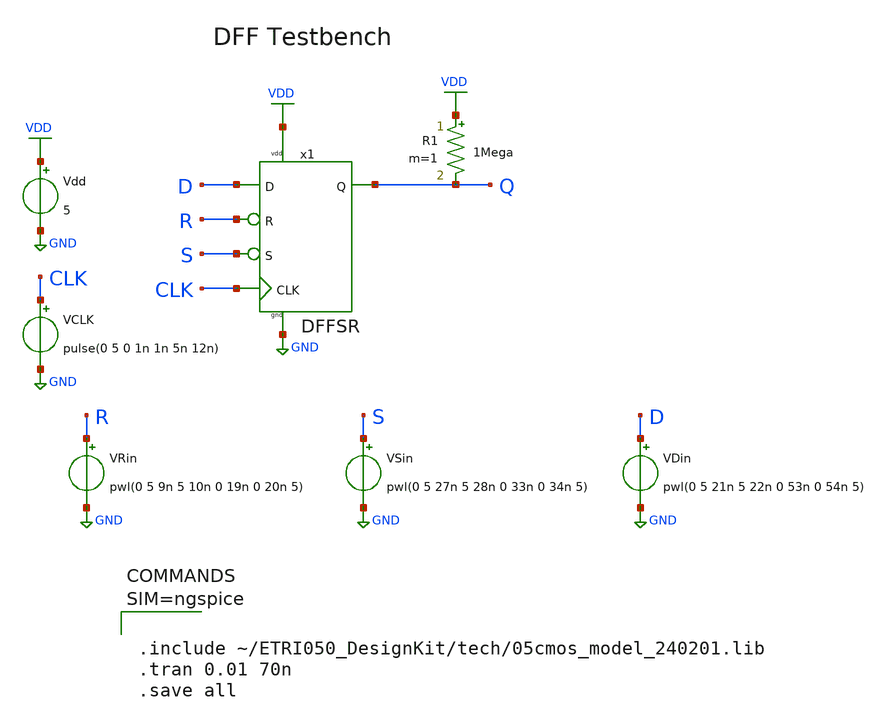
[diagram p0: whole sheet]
** sch_path: Tutorials/1-4_StdCell_DFFSR/Sch/DFFSR_TB.sch
**.subckt DFFSR_TB
Vdd VDD GND 5
VDin D GND pwl(0 5 21n 5 22n 0 53n 0 54n 5)
VRin R GND pwl(0 5 9n 5 10n 0 19n 0 20n 5)
VSin S GND pwl(0 5 27n 5 28n 0 33n 0 34n 5)
VCLK CLK GND pulse(0 5 0 1n 1n 5n 12n)
R1 VDD Q 1Mega m=1
x1 D R S CLK Q VDD GND DFFSR
**** begin user architecture code



.include ~/ETRI050_DesignKit/tech/05cmos_model_240201.lib
.tran 0.01 70n
.save all



**** end user architecture code
**.ends

* expanding   symbol:  /home/goodkook/ETRI050_DesignKit/Tutorials/1-4_StdCell_DFFSR/Sch/DFFSR.sym #
*+ of pins=7
** sym_path: Tutorials/1-4_StdCell_DFFSR/Sch/DFFSR.sym
** sch_path: Tutorials/1-4_StdCell_DFFSR/Sch/DFFSR.sch
.subckt DFFSR D R S CLK Q vdd gnd
*.ipin CLK
*.ipin D
*.opin Q
*.ipin S
*.ipin R
*.iopin vdd
*.iopin gnd
M1 net1 C_Bar net2 VDD pfet w=3u l=0.6u m=1
M2 net1 C net2 GND nfet w=3u l=0.6u m=1
M3 net5 C net2 VDD pfet w=3u l=0.6u m=1
M4 net5 C_Bar net2 GND nfet w=3u l=0.6u m=1
M6 net4 C_Bar net3 VDD pfet w=3u l=0.6u m=1
M5 net4 C net3 GND nfet w=3u l=0.6u m=1
M7 net4 C net6 VDD pfet w=3u l=0.6u m=1
M8 net4 C_Bar net6 GND nfet w=3u l=0.6u m=1
x1 CLK C_Bar vdd gnd INVX1
x2 C_Bar C vdd gnd INVX1
x4 net2 S net3 vdd gnd NAND2X1
x6 net3 R net1 vdd gnd NAND2X1
x7 net4 R net7 vdd gnd NAND2X1
x8 S net7 net6 vdd gnd NAND2X1
x3 D net5 vdd gnd INVX1
x5 net7 Q vdd gnd INVX1
.ends


* expanding   symbol:  /home/goodkook/ETRI050_DesignKit/Tutorials/1-4_StdCell_DFFSR/Sch/INVX1.sym #
*+ of pins=4
** sym_path: Tutorials/1-4_StdCell_DFFSR/Sch/INVX1.sym
** sch_path: Tutorials/1-4_StdCell_DFFSR/Sch/INVX1.sch
.subckt INVX1 A Y vdd gnd
*.ipin A
*.opin Y
*.iopin vdd
*.iopin gnd
M1 Y A gnd GND nfet w=3u l=0.6u m=1
M2 Y A vdd VDD pfet w=6u l=0.6u m=1
.ends


* expanding   symbol:  /home/goodkook/ETRI050_DesignKit/Tutorials/1-4_StdCell_DFFSR/Sch/NAND2X1.sym
*+ # of pins=5
** sym_path: Tutorials/1-4_StdCell_DFFSR/Sch/NAND2X1.sym
** sch_path: Tutorials/1-4_StdCell_DFFSR/Sch/NAND2X1.sch
.subckt NAND2X1 A B Y vdd gnd
*.ipin A
*.ipin B
*.opin Y
*.iopin vdd
*.iopin gnd
M1 Y B net1 GND nfet w=6u l=0.6u m=1
M2 Y B vdd VDD pfet w=6u l=0.6u m=1
M3 net1 A gnd GND nfet w=6u l=0.6u m=1
M4 Y A vdd VDD pfet w=6u l=0.6u m=1
.ends

.GLOBAL VDD
.GLOBAL GND
.end
